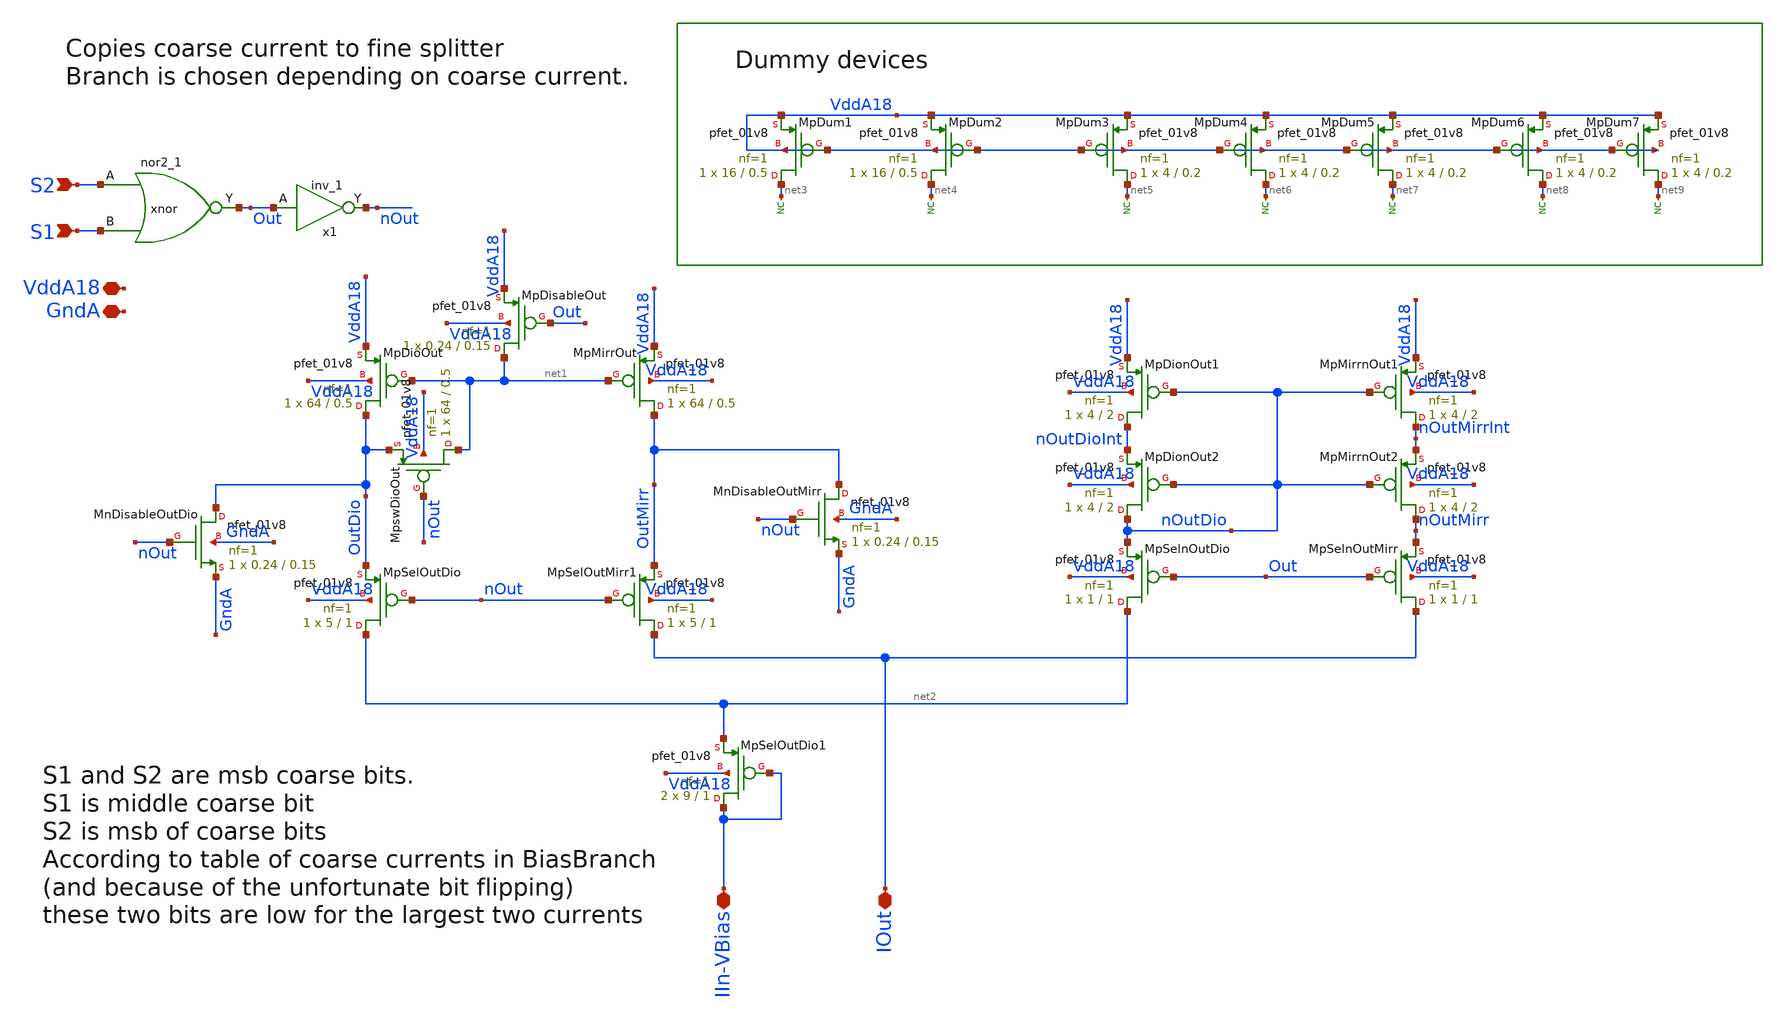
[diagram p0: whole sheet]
** sch_path: analog/xschem/BiasCoarseFineInterface.sch
**.subckt BiasCoarseFineInterface GndA VddA18 IIn-VBias IOut S2 S1
*.iopin GndA
*.iopin VddA18
*.iopin IIn-VBias
*.iopin IOut
*.ipin S2
*.ipin S1
XMpDisableOut net1 Out VddA18 VddA18 sky130_fd_pr__pfet_01v8 L=0.15 W=0.24 nf=1 ad='int((1 + 1)/2) * 0.24 / 1 * 0.29'
+ as='int((1 + 2)/2) * 0.24 / 1 * 0.29' pd='2*int((1 + 1)/2) * (0.24 / 1 + 0.29)' ps='2*int((1 + 2)/2) * (0.24 / 1 + 0.29)'
+ nrd='0.29 / 0.24 ' nrs='0.29 / 0.24 ' sa=0 sb=0 sd=0 mult=1 m=1
XMpDioOut OutDio net1 VddA18 VddA18 sky130_fd_pr__pfet_01v8 L=0.5 W=64 nf=1 ad='int((1 + 1)/2) * 64 / 1 * 0.29'
+ as='int((1 + 2)/2) * 64 / 1 * 0.29' pd='2*int((1 + 1)/2) * (64 / 1 + 0.29)' ps='2*int((1 + 2)/2) * (64 / 1 + 0.29)'
+ nrd='0.29 / 64 ' nrs='0.29 / 64 ' sa=0 sb=0 sd=0 mult=1 m=1
XMpMirrOut OutMirr net1 VddA18 VddA18 sky130_fd_pr__pfet_01v8 L=0.5 W=64 nf=1 ad='int((1 + 1)/2) * 64 / 1 * 0.29'
+ as='int((1 + 2)/2) * 64 / 1 * 0.29' pd='2*int((1 + 1)/2) * (64 / 1 + 0.29)' ps='2*int((1 + 2)/2) * (64 / 1 + 0.29)'
+ nrd='0.29 / 64 ' nrs='0.29 / 64 ' sa=0 sb=0 sd=0 mult=1 m=1
XMpswDioOut net1 nOut OutDio VddA18 sky130_fd_pr__pfet_01v8 L=0.5 W=64 nf=1 ad='int((1 + 1)/2) * 64 / 1 * 0.29'
+ as='int((1 + 2)/2) * 64 / 1 * 0.29' pd='2*int((1 + 1)/2) * (64 / 1 + 0.29)' ps='2*int((1 + 2)/2) * (64 / 1 + 0.29)'
+ nrd='0.29 / 64 ' nrs='0.29 / 64 ' sa=0 sb=0 sd=0 mult=1 m=1
XMnDisableOutDio OutDio nOut GndA GndA sky130_fd_pr__nfet_01v8 L=0.15 W=0.24 nf=1 ad='int((1 + 1)/2) * 0.24 / 1 * 0.29'
+ as='int((1 + 2)/2) * 0.24 / 1 * 0.29' pd='2*int((1 + 1)/2) * (0.24 / 1 + 0.29)' ps='2*int((1 + 2)/2) * (0.24 / 1 + 0.29)'
+ nrd='0.29 / 0.24 ' nrs='0.29 / 0.24 ' sa=0 sb=0 sd=0 mult=1 m=1
XMpSelOutDio net2 nOut OutDio VddA18 sky130_fd_pr__pfet_01v8 L=1 W=5 nf=1 ad='int((1 + 1)/2) * 5 / 1 * 0.29'
+ as='int((1 + 2)/2) * 5 / 1 * 0.29' pd='2*int((1 + 1)/2) * (5 / 1 + 0.29)' ps='2*int((1 + 2)/2) * (5 / 1 + 0.29)'
+ nrd='0.29 / 5 ' nrs='0.29 / 5 ' sa=0 sb=0 sd=0 mult=1 m=1
XMpSelOutMirr1 IOut nOut OutMirr VddA18 sky130_fd_pr__pfet_01v8 L=1 W=5 nf=1 ad='int((1 + 1)/2) * 5 / 1 * 0.29'
+ as='int((1 + 2)/2) * 5 / 1 * 0.29' pd='2*int((1 + 1)/2) * (5 / 1 + 0.29)' ps='2*int((1 + 2)/2) * (5 / 1 + 0.29)'
+ nrd='0.29 / 5 ' nrs='0.29 / 5 ' sa=0 sb=0 sd=0 mult=1 m=1
XMnDisableOutMirr OutMirr nOut GndA GndA sky130_fd_pr__nfet_01v8 L=0.15 W=0.24 nf=1 ad='int((1 + 1)/2) * 0.24 / 1 * 0.29'
+ as='int((1 + 2)/2) * 0.24 / 1 * 0.29' pd='2*int((1 + 1)/2) * (0.24 / 1 + 0.29)' ps='2*int((1 + 2)/2) * (0.24 / 1 + 0.29)'
+ nrd='0.29 / 0.24 ' nrs='0.29 / 0.24 ' sa=0 sb=0 sd=0 mult=1 m=1
XMpSelOutDio1 IIn-VBias IIn-VBias net2 VddA18 sky130_fd_pr__pfet_01v8 L=1 W=9 nf=1 ad='int((1 + 1)/2) * 9 / 1 * 0.29'
+ as='int((1 + 2)/2) * 9 / 1 * 0.29' pd='2*int((1 + 1)/2) * (9 / 1 + 0.29)' ps='2*int((1 + 2)/2) * (9 / 1 + 0.29)'
+ nrd='0.29 / 9 ' nrs='0.29 / 9 ' sa=0 sb=0 sd=0 mult=2 m=2
XMpDionOut1 nOutDioInt nOutDio VddA18 VddA18 sky130_fd_pr__pfet_01v8 L=2 W=4 nf=1 ad='int((1 + 1)/2) * 4 / 1 * 0.29'
+ as='int((1 + 2)/2) * 4 / 1 * 0.29' pd='2*int((1 + 1)/2) * (4 / 1 + 0.29)' ps='2*int((1 + 2)/2) * (4 / 1 + 0.29)'
+ nrd='0.29 / 4 ' nrs='0.29 / 4 ' sa=0 sb=0 sd=0 mult=1 m=1
XMpMirrnOut1 nOutMirrInt nOutDio VddA18 VddA18 sky130_fd_pr__pfet_01v8 L=2 W=4 nf=1 ad='int((1 + 1)/2) * 4 / 1 * 0.29'
+ as='int((1 + 2)/2) * 4 / 1 * 0.29' pd='2*int((1 + 1)/2) * (4 / 1 + 0.29)' ps='2*int((1 + 2)/2) * (4 / 1 + 0.29)'
+ nrd='0.29 / 4 ' nrs='0.29 / 4 ' sa=0 sb=0 sd=0 mult=1 m=1
XMpDionOut2 nOutDio nOutDio nOutDioInt VddA18 sky130_fd_pr__pfet_01v8 L=2 W=4 nf=1 ad='int((1 + 1)/2) * 4 / 1 * 0.29'
+ as='int((1 + 2)/2) * 4 / 1 * 0.29' pd='2*int((1 + 1)/2) * (4 / 1 + 0.29)' ps='2*int((1 + 2)/2) * (4 / 1 + 0.29)'
+ nrd='0.29 / 4 ' nrs='0.29 / 4 ' sa=0 sb=0 sd=0 mult=1 m=1
XMpMirrnOut2 nOutMirr nOutDio nOutMirrInt VddA18 sky130_fd_pr__pfet_01v8 L=2 W=4 nf=1 ad='int((1 + 1)/2) * 4 / 1 * 0.29'
+ as='int((1 + 2)/2) * 4 / 1 * 0.29' pd='2*int((1 + 1)/2) * (4 / 1 + 0.29)' ps='2*int((1 + 2)/2) * (4 / 1 + 0.29)'
+ nrd='0.29 / 4 ' nrs='0.29 / 4 ' sa=0 sb=0 sd=0 mult=1 m=1
XMpSelnOutDio net2 Out nOutDio VddA18 sky130_fd_pr__pfet_01v8 L=1 W=1 nf=1 ad='int((1 + 1)/2) * 1 / 1 * 0.29'
+ as='int((1 + 2)/2) * 1 / 1 * 0.29' pd='2*int((1 + 1)/2) * (1 / 1 + 0.29)' ps='2*int((1 + 2)/2) * (1 / 1 + 0.29)'
+ nrd='0.29 / 1 ' nrs='0.29 / 1 ' sa=0 sb=0 sd=0 mult=1 m=1
XMpSelnOutMirr IOut Out nOutMirr VddA18 sky130_fd_pr__pfet_01v8 L=1 W=1 nf=1 ad='int((1 + 1)/2) * 1 / 1 * 0.29'
+ as='int((1 + 2)/2) * 1 / 1 * 0.29' pd='2*int((1 + 1)/2) * (1 / 1 + 0.29)' ps='2*int((1 + 2)/2) * (1 / 1 + 0.29)'
+ nrd='0.29 / 1 ' nrs='0.29 / 1 ' sa=0 sb=0 sd=0 mult=1 m=1
XMpDum1 net3 VddA18 VddA18 VddA18 sky130_fd_pr__pfet_01v8 L=0.5 W=16 nf=1 ad='int((1 + 1)/2) * 16 / 1 * 0.29'
+ as='int((1 + 2)/2) * 16 / 1 * 0.29' pd='2*int((1 + 1)/2) * (16 / 1 + 0.29)' ps='2*int((1 + 2)/2) * (16 / 1 + 0.29)'
+ nrd='0.29 / 16 ' nrs='0.29 / 16 ' sa=0 sb=0 sd=0 mult=1 m=1
XMpDum2 net4 VddA18 VddA18 VddA18 sky130_fd_pr__pfet_01v8 L=0.5 W=16 nf=1 ad='int((1 + 1)/2) * 16 / 1 * 0.29'
+ as='int((1 + 2)/2) * 16 / 1 * 0.29' pd='2*int((1 + 1)/2) * (16 / 1 + 0.29)' ps='2*int((1 + 2)/2) * (16 / 1 + 0.29)'
+ nrd='0.29 / 16 ' nrs='0.29 / 16 ' sa=0 sb=0 sd=0 mult=1 m=1
XMpDum3 net5 VddA18 VddA18 VddA18 sky130_fd_pr__pfet_01v8 L=0.2 W=4 nf=1 ad='int((1 + 1)/2) * 4 / 1 * 0.29'
+ as='int((1 + 2)/2) * 4 / 1 * 0.29' pd='2*int((1 + 1)/2) * (4 / 1 + 0.29)' ps='2*int((1 + 2)/2) * (4 / 1 + 0.29)'
+ nrd='0.29 / 4 ' nrs='0.29 / 4 ' sa=0 sb=0 sd=0 mult=1 m=1
XMpDum4 net6 VddA18 VddA18 VddA18 sky130_fd_pr__pfet_01v8 L=0.2 W=4 nf=1 ad='int((1 + 1)/2) * 4 / 1 * 0.29'
+ as='int((1 + 2)/2) * 4 / 1 * 0.29' pd='2*int((1 + 1)/2) * (4 / 1 + 0.29)' ps='2*int((1 + 2)/2) * (4 / 1 + 0.29)'
+ nrd='0.29 / 4 ' nrs='0.29 / 4 ' sa=0 sb=0 sd=0 mult=1 m=1
XMpDum5 net7 VddA18 VddA18 VddA18 sky130_fd_pr__pfet_01v8 L=0.2 W=4 nf=1 ad='int((1 + 1)/2) * 4 / 1 * 0.29'
+ as='int((1 + 2)/2) * 4 / 1 * 0.29' pd='2*int((1 + 1)/2) * (4 / 1 + 0.29)' ps='2*int((1 + 2)/2) * (4 / 1 + 0.29)'
+ nrd='0.29 / 4 ' nrs='0.29 / 4 ' sa=0 sb=0 sd=0 mult=1 m=1
XMpDum6 net8 VddA18 VddA18 VddA18 sky130_fd_pr__pfet_01v8 L=0.2 W=4 nf=1 ad='int((1 + 1)/2) * 4 / 1 * 0.29'
+ as='int((1 + 2)/2) * 4 / 1 * 0.29' pd='2*int((1 + 1)/2) * (4 / 1 + 0.29)' ps='2*int((1 + 2)/2) * (4 / 1 + 0.29)'
+ nrd='0.29 / 4 ' nrs='0.29 / 4 ' sa=0 sb=0 sd=0 mult=1 m=1
XMpDum7 net9 VddA18 VddA18 VddA18 sky130_fd_pr__pfet_01v8 L=0.2 W=4 nf=1 ad='int((1 + 1)/2) * 4 / 1 * 0.29'
+ as='int((1 + 2)/2) * 4 / 1 * 0.29' pd='2*int((1 + 1)/2) * (4 / 1 + 0.29)' ps='2*int((1 + 2)/2) * (4 / 1 + 0.29)'
+ nrd='0.29 / 4 ' nrs='0.29 / 4 ' sa=0 sb=0 sd=0 mult=1 m=1
* noconn #net3
* noconn #net4
* noconn #net5
* noconn #net6
* noconn #net7
* noconn #net8
* noconn #net9
xnor S2 S1 GndA GndA VddA18 VddA18 Out sky130_fd_sc_hd__nor2_1
x1 Out GndA GndA VddA18 VddA18 nOut sky130_fd_sc_hd__inv_1
**.ends
.end
